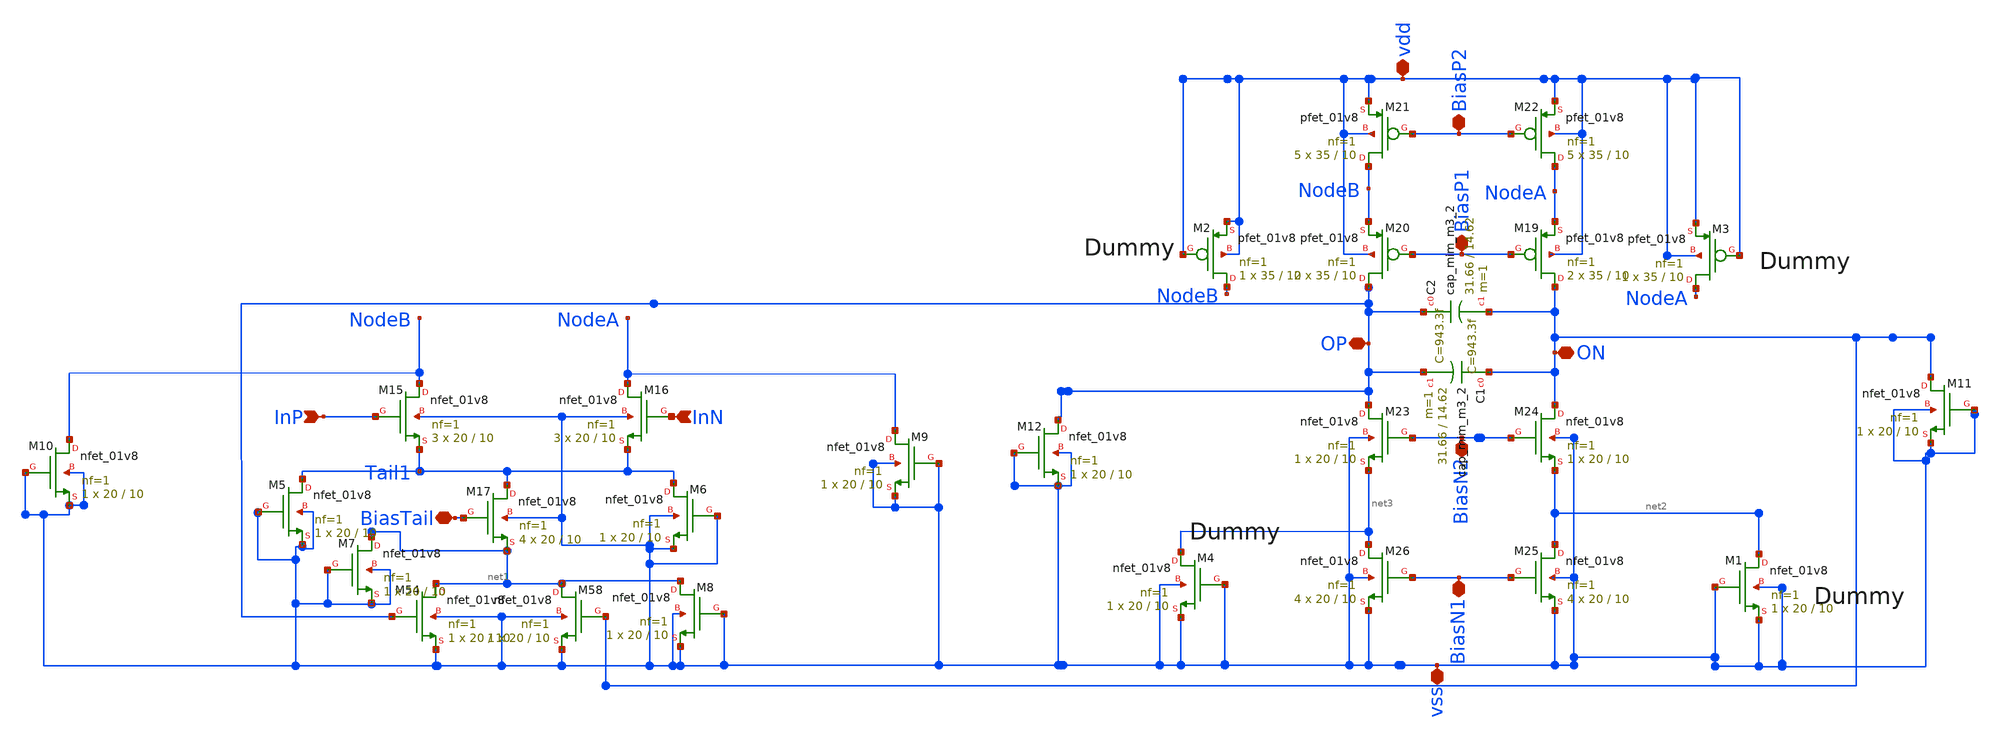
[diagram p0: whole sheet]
** sch_path: xschem/integrator_c.sch
**.subckt integrator_c vss BiasN1 BiasN2 BiasP1 BiasP2 vdd BiasTail ON OP InP InN
*.iopin vss
*.iopin BiasN1
*.iopin BiasN2
*.iopin BiasP1
*.iopin BiasP2
*.iopin vdd
*.iopin BiasTail
*.iopin ON
*.iopin OP
*.ipin InP
*.ipin InN
XM15 NodeB InP Tail1 vss sky130_fd_pr__nfet_01v8 L=10 W=20 nf=1 ad='int((nf+1)/2) * W/nf * 0.29' as='int((nf+2)/2) * W/nf * 0.29'
+ pd='2*int((nf+1)/2) * (W/nf + 0.29)' ps='2*int((nf+2)/2) * (W/nf + 0.29)' nrd='0.29 / W' nrs='0.29 / W'
+ sa=0 sb=0 sd=0 mult=3 m=3
XM16 NodeA InN Tail1 vss sky130_fd_pr__nfet_01v8 L=10 W=20 nf=1 ad='int((nf+1)/2) * W/nf * 0.29' as='int((nf+2)/2) * W/nf * 0.29'
+ pd='2*int((nf+1)/2) * (W/nf + 0.29)' ps='2*int((nf+2)/2) * (W/nf + 0.29)' nrd='0.29 / W' nrs='0.29 / W'
+ sa=0 sb=0 sd=0 mult=3 m=3
XM17 Tail1 BiasTail net1 vss sky130_fd_pr__nfet_01v8 L=10 W=20 nf=1 ad='int((nf+1)/2) * W/nf * 0.29'
+ as='int((nf+2)/2) * W/nf * 0.29' pd='2*int((nf+1)/2) * (W/nf + 0.29)' ps='2*int((nf+2)/2) * (W/nf + 0.29)'
+ nrd='0.29 / W' nrs='0.29 / W' sa=0 sb=0 sd=0 mult=4 m=4
XM19 ON BiasP1 NodeA vdd sky130_fd_pr__pfet_01v8 L=10 W=35 nf=1 ad='int((nf+1)/2) * W/nf * 0.29' as='int((nf+2)/2) * W/nf * 0.29'
+ pd='2*int((nf+1)/2) * (W/nf + 0.29)' ps='2*int((nf+2)/2) * (W/nf + 0.29)' nrd='0.29 / W' nrs='0.29 / W'
+ sa=0 sb=0 sd=0 mult=2 m=2
XM20 OP BiasP1 NodeB vdd sky130_fd_pr__pfet_01v8 L=10 W=35 nf=1 ad='int((nf+1)/2) * W/nf * 0.29' as='int((nf+2)/2) * W/nf * 0.29'
+ pd='2*int((nf+1)/2) * (W/nf + 0.29)' ps='2*int((nf+2)/2) * (W/nf + 0.29)' nrd='0.29 / W' nrs='0.29 / W'
+ sa=0 sb=0 sd=0 mult=2 m=2
XM21 NodeB BiasP2 vdd vdd sky130_fd_pr__pfet_01v8 L=10 W=35 nf=1 ad='int((nf+1)/2) * W/nf * 0.29' as='int((nf+2)/2) * W/nf * 0.29'
+ pd='2*int((nf+1)/2) * (W/nf + 0.29)' ps='2*int((nf+2)/2) * (W/nf + 0.29)' nrd='0.29 / W' nrs='0.29 / W'
+ sa=0 sb=0 sd=0 mult=5 m=5
XM22 NodeA BiasP2 vdd vdd sky130_fd_pr__pfet_01v8 L=10 W=35 nf=1 ad='int((nf+1)/2) * W/nf * 0.29' as='int((nf+2)/2) * W/nf * 0.29'
+ pd='2*int((nf+1)/2) * (W/nf + 0.29)' ps='2*int((nf+2)/2) * (W/nf + 0.29)' nrd='0.29 / W' nrs='0.29 / W'
+ sa=0 sb=0 sd=0 mult=5 m=5
XM23 OP BiasN2 net3 vss sky130_fd_pr__nfet_01v8 L=10 W=20 nf=1 ad='int((nf+1)/2) * W/nf * 0.29' as='int((nf+2)/2) * W/nf * 0.29'
+ pd='2*int((nf+1)/2) * (W/nf + 0.29)' ps='2*int((nf+2)/2) * (W/nf + 0.29)' nrd='0.29 / W' nrs='0.29 / W'
+ sa=0 sb=0 sd=0 mult=1 m=1
XM24 ON BiasN2 net2 vss sky130_fd_pr__nfet_01v8 L=10 W=20 nf=1 ad='int((nf+1)/2) * W/nf * 0.29' as='int((nf+2)/2) * W/nf * 0.29'
+ pd='2*int((nf+1)/2) * (W/nf + 0.29)' ps='2*int((nf+2)/2) * (W/nf + 0.29)' nrd='0.29 / W' nrs='0.29 / W'
+ sa=0 sb=0 sd=0 mult=1 m=1
XM25 net2 BiasN1 vss vss sky130_fd_pr__nfet_01v8 L=10 W=20 nf=1 ad='int((nf+1)/2) * W/nf * 0.29' as='int((nf+2)/2) * W/nf * 0.29'
+ pd='2*int((nf+1)/2) * (W/nf + 0.29)' ps='2*int((nf+2)/2) * (W/nf + 0.29)' nrd='0.29 / W' nrs='0.29 / W'
+ sa=0 sb=0 sd=0 mult=4 m=4
XM26 net3 BiasN1 vss vss sky130_fd_pr__nfet_01v8 L=10 W=20 nf=1 ad='int((nf+1)/2) * W/nf * 0.29' as='int((nf+2)/2) * W/nf * 0.29'
+ pd='2*int((nf+1)/2) * (W/nf + 0.29)' ps='2*int((nf+2)/2) * (W/nf + 0.29)' nrd='0.29 / W' nrs='0.29 / W'
+ sa=0 sb=0 sd=0 mult=4 m=4
XM54 net1 OP vss vss sky130_fd_pr__nfet_01v8 L=10 W=20 nf=1 ad='int((nf+1)/2) * W/nf * 0.29' as='int((nf+2)/2) * W/nf * 0.29'
+ pd='2*int((nf+1)/2) * (W/nf + 0.29)' ps='2*int((nf+2)/2) * (W/nf + 0.29)' nrd='0.29 / W' nrs='0.29 / W'
+ sa=0 sb=0 sd=0 mult=1 m=1
XM58 net1 ON vss vss sky130_fd_pr__nfet_01v8 L=10 W=20 nf=1 ad='int((nf+1)/2) * W/nf * 0.29' as='int((nf+2)/2) * W/nf * 0.29'
+ pd='2*int((nf+1)/2) * (W/nf + 0.29)' ps='2*int((nf+2)/2) * (W/nf + 0.29)' nrd='0.29 / W' nrs='0.29 / W'
+ sa=0 sb=0 sd=0 mult=1 m=1
XM1 net2 vss vss vss sky130_fd_pr__nfet_01v8 L=10 W=20 nf=1 ad='int((nf+1)/2) * W/nf * 0.29' as='int((nf+2)/2) * W/nf * 0.29'
+ pd='2*int((nf+1)/2) * (W/nf + 0.29)' ps='2*int((nf+2)/2) * (W/nf + 0.29)' nrd='0.29 / W' nrs='0.29 / W'
+ sa=0 sb=0 sd=0 mult=1 m=1
XM2 NodeB vdd vdd vdd sky130_fd_pr__pfet_01v8 L=10 W=35 nf=1 ad='int((nf+1)/2) * W/nf * 0.29' as='int((nf+2)/2) * W/nf * 0.29'
+ pd='2*int((nf+1)/2) * (W/nf + 0.29)' ps='2*int((nf+2)/2) * (W/nf + 0.29)' nrd='0.29 / W' nrs='0.29 / W'
+ sa=0 sb=0 sd=0 mult=1 m=1
XM3 NodeA vdd vdd vdd sky130_fd_pr__pfet_01v8 L=10 W=35 nf=1 ad='int((nf+1)/2) * W/nf * 0.29' as='int((nf+2)/2) * W/nf * 0.29'
+ pd='2*int((nf+1)/2) * (W/nf + 0.29)' ps='2*int((nf+2)/2) * (W/nf + 0.29)' nrd='0.29 / W' nrs='0.29 / W'
+ sa=0 sb=0 sd=0 mult=1 m=1
XM4 net3 vss vss vss sky130_fd_pr__nfet_01v8 L=10 W=20 nf=1 ad='int((nf+1)/2) * W/nf * 0.29' as='int((nf+2)/2) * W/nf * 0.29'
+ pd='2*int((nf+1)/2) * (W/nf + 0.29)' ps='2*int((nf+2)/2) * (W/nf + 0.29)' nrd='0.29 / W' nrs='0.29 / W'
+ sa=0 sb=0 sd=0 mult=1 m=1
XM5 Tail1 vss vss vss sky130_fd_pr__nfet_01v8 L=10 W=20 nf=1 ad='int((nf+1)/2) * W/nf * 0.29' as='int((nf+2)/2) * W/nf * 0.29'
+ pd='2*int((nf+1)/2) * (W/nf + 0.29)' ps='2*int((nf+2)/2) * (W/nf + 0.29)' nrd='0.29 / W' nrs='0.29 / W'
+ sa=0 sb=0 sd=0 mult=1 m=1
XM6 Tail1 vss vss vss sky130_fd_pr__nfet_01v8 L=10 W=20 nf=1 ad='int((nf+1)/2) * W/nf * 0.29' as='int((nf+2)/2) * W/nf * 0.29'
+ pd='2*int((nf+1)/2) * (W/nf + 0.29)' ps='2*int((nf+2)/2) * (W/nf + 0.29)' nrd='0.29 / W' nrs='0.29 / W'
+ sa=0 sb=0 sd=0 mult=1 m=1
XM7 net1 vss vss vss sky130_fd_pr__nfet_01v8 L=10 W=20 nf=1 ad='int((nf+1)/2) * W/nf * 0.29' as='int((nf+2)/2) * W/nf * 0.29'
+ pd='2*int((nf+1)/2) * (W/nf + 0.29)' ps='2*int((nf+2)/2) * (W/nf + 0.29)' nrd='0.29 / W' nrs='0.29 / W'
+ sa=0 sb=0 sd=0 mult=1 m=1
XM8 net1 vss vss vss sky130_fd_pr__nfet_01v8 L=10 W=20 nf=1 ad='int((nf+1)/2) * W/nf * 0.29' as='int((nf+2)/2) * W/nf * 0.29'
+ pd='2*int((nf+1)/2) * (W/nf + 0.29)' ps='2*int((nf+2)/2) * (W/nf + 0.29)' nrd='0.29 / W' nrs='0.29 / W'
+ sa=0 sb=0 sd=0 mult=1 m=1
XM9 NodeA vss vss vss sky130_fd_pr__nfet_01v8 L=10 W=20 nf=1 ad='int((nf+1)/2) * W/nf * 0.29' as='int((nf+2)/2) * W/nf * 0.29'
+ pd='2*int((nf+1)/2) * (W/nf + 0.29)' ps='2*int((nf+2)/2) * (W/nf + 0.29)' nrd='0.29 / W' nrs='0.29 / W'
+ sa=0 sb=0 sd=0 mult=1 m=1
XM10 NodeB vss vss vss sky130_fd_pr__nfet_01v8 L=10 W=20 nf=1 ad='int((nf+1)/2) * W/nf * 0.29' as='int((nf+2)/2) * W/nf * 0.29'
+ pd='2*int((nf+1)/2) * (W/nf + 0.29)' ps='2*int((nf+2)/2) * (W/nf + 0.29)' nrd='0.29 / W' nrs='0.29 / W'
+ sa=0 sb=0 sd=0 mult=1 m=1
XM11 ON vss vss vss sky130_fd_pr__nfet_01v8 L=10 W=20 nf=1 ad='int((nf+1)/2) * W/nf * 0.29' as='int((nf+2)/2) * W/nf * 0.29'
+ pd='2*int((nf+1)/2) * (W/nf + 0.29)' ps='2*int((nf+2)/2) * (W/nf + 0.29)' nrd='0.29 / W' nrs='0.29 / W'
+ sa=0 sb=0 sd=0 mult=1 m=1
XM12 OP vss vss vss sky130_fd_pr__nfet_01v8 L=10 W=20 nf=1 ad='int((nf+1)/2) * W/nf * 0.29' as='int((nf+2)/2) * W/nf * 0.29'
+ pd='2*int((nf+1)/2) * (W/nf + 0.29)' ps='2*int((nf+2)/2) * (W/nf + 0.29)' nrd='0.29 / W' nrs='0.29 / W'
+ sa=0 sb=0 sd=0 mult=1 m=1
XC1 ON OP sky130_fd_pr__cap_mim_m3_2 W=31.66 L=14.62 MF=1 m=1
XC2 OP ON sky130_fd_pr__cap_mim_m3_2 W=31.66 L=14.62 MF=1 m=1
**.ends
.end
